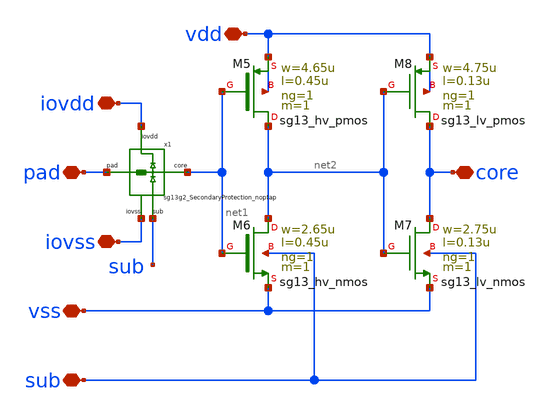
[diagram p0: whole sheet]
** sch_path: ihp-sg13g2/sg13g2_io/xschem/sg13g2_LevelDown_noptap.sch
**.subckt sg13g2_LevelDown_noptap iovdd vss core pad vdd iovss sub
*.iopin iovdd
*.iopin vss
*.iopin core
*.iopin pad
*.iopin vdd
*.iopin iovss
*.iopin sub
XM5 net2 net1 vdd vdd sg13_hv_pmos w=4.65u l=0.45u ng=1 m=1 mm_ok=1
XM6 net2 net1 vss sub sg13_hv_nmos w=2.65u l=0.45u ng=1 m=1 mm_ok=1
XM7 core net2 vss sub sg13_lv_nmos w=2.75u l=0.13u ng=1 m=1 mm_ok=1
XM8 core net2 vdd vdd sg13_lv_pmos w=4.75u l=0.13u ng=1 m=1 mm_ok=1
x1 net1 iovdd iovss pad sub sg13g2_SecondaryProtection_noptap
**.ends

* expanding   symbol:  sg13g2_SecondaryProtection_noptap.sym # of pins=5
** sym_path: ihp-sg13g2/sg13g2_io/xschem/sg13g2_SecondaryProtection_noptap.sym
** sch_path: ihp-sg13g2/sg13g2_io/xschem/sg13g2_SecondaryProtection_noptap.sch
.subckt sg13g2_SecondaryProtection_noptap core iovdd iovss pad sub
*.iopin iovss
*.iopin core
*.iopin pad
*.iopin iovdd
*.iopin sub
XD1 core iovdd dpantenna l=4.98u w=0.64u
XR2 core pad sub rppd w=1e-6 l=2e-6 m=1 b=0 mm_ok=1
XD2 sub core dantenna l=3.1u w=0.64u
.ends

.end
